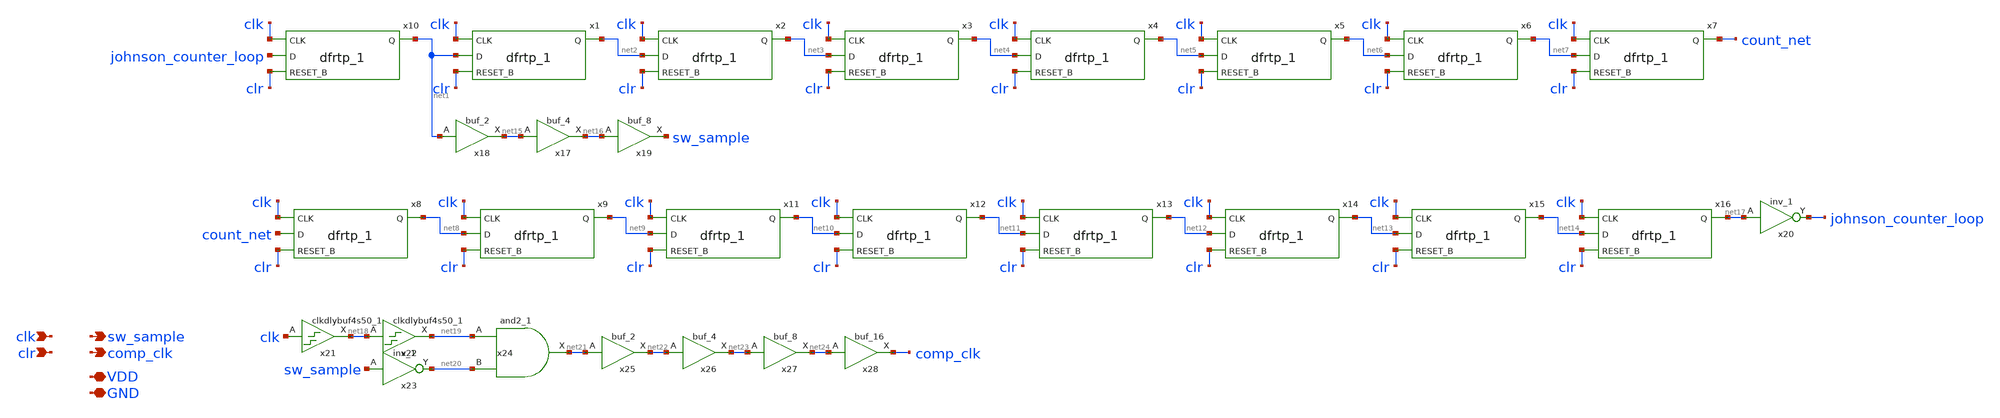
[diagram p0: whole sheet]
** sch_path: xschem/sample_clock.sch
**.subckt sample_clock clk clr VDD GND sw_sample comp_clk
*.ipin clk
*.ipin clr
*.iopin VDD
*.iopin GND
*.opin sw_sample
*.opin comp_clk
x10 clk johnson_counter_loop clr GND GND VDD VDD net1 sky130_fd_sc_hd__dfrtp_1
x1 clk net1 clr GND GND VDD VDD net2 sky130_fd_sc_hd__dfrtp_1
x2 clk net2 clr GND GND VDD VDD net3 sky130_fd_sc_hd__dfrtp_1
x3 clk net3 clr GND GND VDD VDD net4 sky130_fd_sc_hd__dfrtp_1
x4 clk net4 clr GND GND VDD VDD net5 sky130_fd_sc_hd__dfrtp_1
x5 clk net5 clr GND GND VDD VDD net6 sky130_fd_sc_hd__dfrtp_1
x6 clk net6 clr GND GND VDD VDD net7 sky130_fd_sc_hd__dfrtp_1
x7 clk net7 clr GND GND VDD VDD count_net sky130_fd_sc_hd__dfrtp_1
x8 clk count_net clr GND GND VDD VDD net8 sky130_fd_sc_hd__dfrtp_1
x9 clk net8 clr GND GND VDD VDD net9 sky130_fd_sc_hd__dfrtp_1
x11 clk net9 clr GND GND VDD VDD net10 sky130_fd_sc_hd__dfrtp_1
x12 clk net10 clr GND GND VDD VDD net11 sky130_fd_sc_hd__dfrtp_1
x13 clk net11 clr GND GND VDD VDD net12 sky130_fd_sc_hd__dfrtp_1
x14 clk net12 clr GND GND VDD VDD net13 sky130_fd_sc_hd__dfrtp_1
x15 clk net13 clr GND GND VDD VDD net14 sky130_fd_sc_hd__dfrtp_1
x16 clk net14 clr GND GND VDD VDD net17 sky130_fd_sc_hd__dfrtp_1
x17 net15 GND GND VDD VDD net16 sky130_fd_sc_hd__buf_4
x18 net1 GND GND VDD VDD net15 sky130_fd_sc_hd__buf_2
x19 net16 GND GND VDD VDD sw_sample sky130_fd_sc_hd__buf_8
x20 net17 GND GND VDD VDD johnson_counter_loop sky130_fd_sc_hd__inv_1
x22 net18 GND GND VDD VDD net19 sky130_fd_sc_hd__clkdlybuf4s50_1
x23 sw_sample GND GND VDD VDD net20 sky130_fd_sc_hd__inv_1
x24 net19 net20 GND GND VDD VDD net21 sky130_fd_sc_hd__and2_1
x25 net21 GND GND VDD VDD net22 sky130_fd_sc_hd__buf_2
x26 net22 GND GND VDD VDD net23 sky130_fd_sc_hd__buf_4
x27 net23 GND GND VDD VDD net24 sky130_fd_sc_hd__buf_8
x21 clk GND GND VDD VDD net18 sky130_fd_sc_hd__clkdlybuf4s50_1
x28 net24 GND GNB VDD VDD comp_clk sky130_fd_sc_hd__buf_16
**.ends
.end
